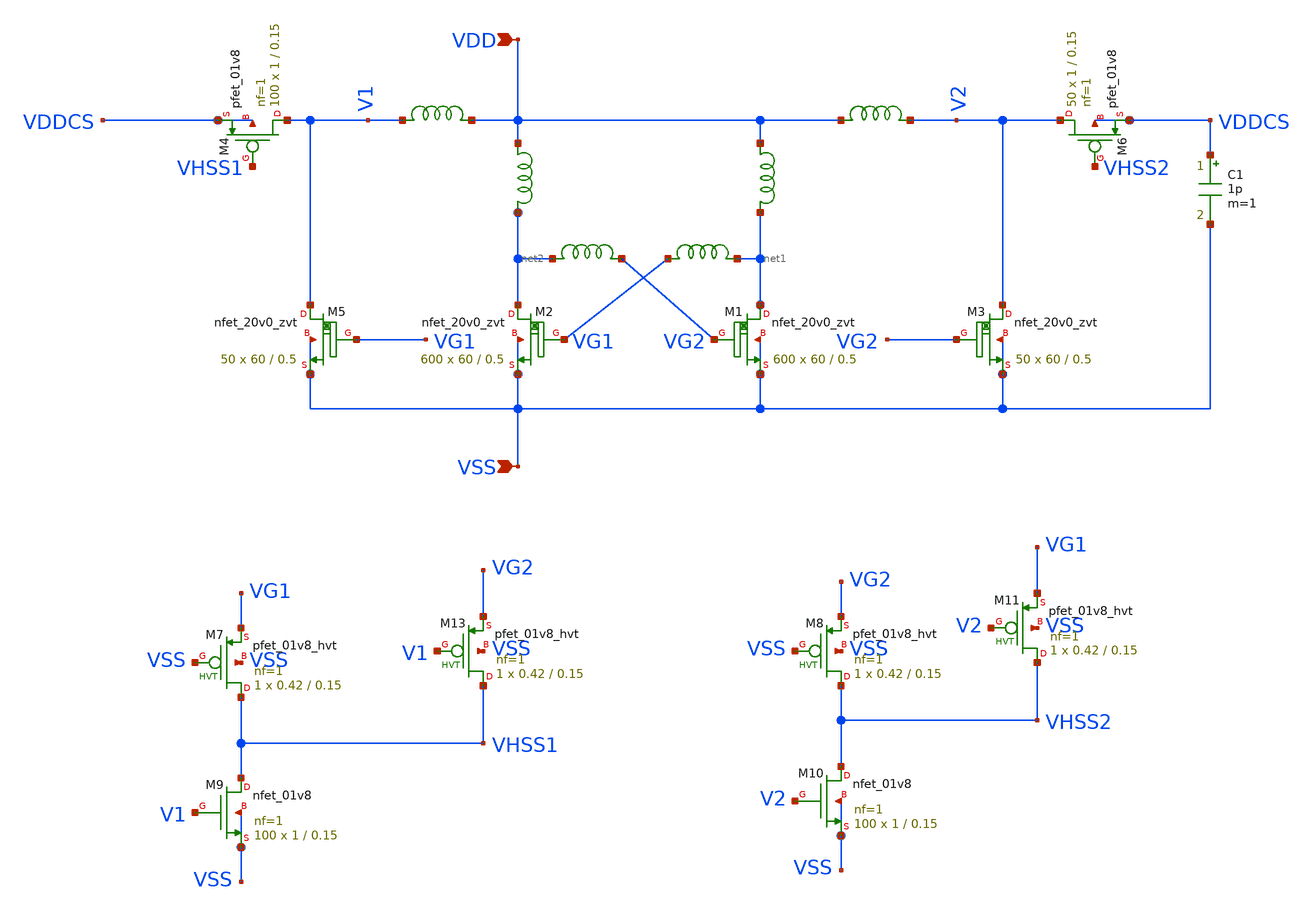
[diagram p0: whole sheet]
** sch_path: design/LELO_SVOD_SKY130A/LELO_EXSC.sch
**.subckt LELO_EXSC VSS VDD
*.ipin VSS
*.ipin VDD
x3 VDD net1 1812PS-102_imp
x4 VDD net2 1812PS-102_imp
XM1 net1 VG2 VSS VSS sky130_fd_pr__nfet_20v0_zvt W=60 L=0.5 m=600
XM2 net2 VG1 VSS VSS sky130_fd_pr__nfet_20v0_zvt W=60 L=0.5 m=600
x1 net2 VG2 1812PS-104_imp
x2 VG1 net1 1812PS-104_imp
XM3 V2 VG2 VSS VSS sky130_fd_pr__nfet_20v0_zvt W=60 L=0.5 m=50
C1 VDDCS VSS 1p m=1
XM5 V1 VG1 VSS VSS sky130_fd_pr__nfet_20v0_zvt W=60 L=0.5 m=50
XM4 V1 VHSS1 VDDCS VDDCS sky130_fd_pr__pfet_01v8 L=0.15 W=1 nf=1 ad='int((1 + 1)/2) * 1 / 1 * 0.29' as='int((1 + 2)/2) * 1 / 1 * 0.29'
+ pd='2*int((1 + 1)/2) * (1 / 1 + 0.29)' ps='2*int((1 + 2)/2) * (1 / 1 + 0.29)' nrd='0.29 / 1 ' nrs='0.29 / 1 '
+ sa=0 sb=0 sd=0 mult=100 m=100
XM6 V2 VHSS2 VDDCS VDDCS sky130_fd_pr__pfet_01v8 L=0.15 W=1 nf=1 ad='int((1 + 1)/2) * 1 / 1 * 0.29' as='int((1 + 2)/2) * 1 / 1 * 0.29'
+ pd='2*int((1 + 1)/2) * (1 / 1 + 0.29)' ps='2*int((1 + 2)/2) * (1 / 1 + 0.29)' nrd='0.29 / 1 ' nrs='0.29 / 1 '
+ sa=0 sb=0 sd=0 mult=50 m=50
XM13 VHSS1 V1 VG2 VSS sky130_fd_pr__pfet_01v8_hvt L=0.15 W=0.42 nf=1 ad='int((1 + 1)/2) * 0.42 / 1 * 0.29'
+ as='int((1 + 2)/2) * 0.42 / 1 * 0.29' pd='2*int((1 + 1)/2) * (0.42 / 1 + 0.29)' ps='2*int((1 + 2)/2) * (0.42 / 1 + 0.29)'
+ nrd='0.29 / 0.42 ' nrs='0.29 / 0.42 ' sa=0 sb=0 sd=0 mult=1 m=1
XM7 VHSS1 VSS VG1 VSS sky130_fd_pr__pfet_01v8_hvt L=0.15 W=0.42 nf=1 ad='int((1 + 1)/2) * 0.42 / 1 * 0.29'
+ as='int((1 + 2)/2) * 0.42 / 1 * 0.29' pd='2*int((1 + 1)/2) * (0.42 / 1 + 0.29)' ps='2*int((1 + 2)/2) * (0.42 / 1 + 0.29)'
+ nrd='0.29 / 0.42 ' nrs='0.29 / 0.42 ' sa=0 sb=0 sd=0 mult=1 m=1
XM8 VHSS2 VSS VG2 VSS sky130_fd_pr__pfet_01v8_hvt L=0.15 W=0.42 nf=1 ad='int((1 + 1)/2) * 0.42 / 1 * 0.29'
+ as='int((1 + 2)/2) * 0.42 / 1 * 0.29' pd='2*int((1 + 1)/2) * (0.42 / 1 + 0.29)' ps='2*int((1 + 2)/2) * (0.42 / 1 + 0.29)'
+ nrd='0.29 / 0.42 ' nrs='0.29 / 0.42 ' sa=0 sb=0 sd=0 mult=1 m=1
XM11 VHSS2 V2 VG1 VSS sky130_fd_pr__pfet_01v8_hvt L=0.15 W=0.42 nf=1 ad='int((1 + 1)/2) * 0.42 / 1 * 0.29'
+ as='int((1 + 2)/2) * 0.42 / 1 * 0.29' pd='2*int((1 + 1)/2) * (0.42 / 1 + 0.29)' ps='2*int((1 + 2)/2) * (0.42 / 1 + 0.29)'
+ nrd='0.29 / 0.42 ' nrs='0.29 / 0.42 ' sa=0 sb=0 sd=0 mult=1 m=1
XM9 VHSS1 V1 VSS VSS sky130_fd_pr__nfet_01v8 L=0.15 W=1 nf=1 ad='int((1 + 1)/2) * 1 / 1 * 0.29' as='int((1 + 2)/2) * 1 / 1 * 0.29'
+ pd='2*int((1 + 1)/2) * (1 / 1 + 0.29)' ps='2*int((1 + 2)/2) * (1 / 1 + 0.29)' nrd='0.29 / 1 ' nrs='0.29 / 1 '
+ sa=0 sb=0 sd=0 mult=100 m=100
XM10 VHSS2 V2 VSS VSS sky130_fd_pr__nfet_01v8 L=0.15 W=1 nf=1 ad='int((1 + 1)/2) * 1 / 1 * 0.29' as='int((1 + 2)/2) * 1 / 1 * 0.29'
+ pd='2*int((1 + 1)/2) * (1 / 1 + 0.29)' ps='2*int((1 + 2)/2) * (1 / 1 + 0.29)' nrd='0.29 / 1 ' nrs='0.29 / 1 '
+ sa=0 sb=0 sd=0 mult=100 m=100
x6 VDD V2 1812PS-334_imp
x5 V1 VDD 1812PS-334_imp
**.ends

* expanding   symbol:  LELO_SVOD_SKY130A/1812PS-102_imp.sym # of pins=2
** sym_path: design/LELO_SVOD_SKY130A/1812PS-102_imp.sym

.subckt 1812PS-102_imp port1 port2
X1 port1 port2 Model1D R1=60 R2=0.054 C= 0.15p K1=0.000001 K2=0.064 K3= 1u K4=1E-06 K5=0.000001 L=0
+ Is=0 a=0 L_Z0=0 L_EL=0 L_F0=0E6 PkZ=1282.46492
.ends 1812PS-102_imp

* expanding   symbol:  LELO_SVOD_SKY130A/1812PS-104_imp.sym # of pins=2
** sym_path: design/LELO_SVOD_SKY130A/1812PS-104_imp.sym

.subckt 1812PS-104_imp port1 port2
X1 port1 port2 Model1D R1=40 R2=1.3 C= 1.6p K1=0.000001 K2=13.98 K3= 100u K4=0.000001 K5=0.000001
+ L=0 Is=0 a=0 L_Z0=0 L_EL=0 L_F0=0E6 PkZ=48065.0165
.ends 1812PS-104_imp

* expanding   symbol:  LELO_SVOD_SKY130A/1812PS-334_imp.sym # of pins=2
** sym_path: design/LELO_SVOD_SKY130A/1812PS-334_imp.sym

.subckt 1812PS-334_imp port1 port2
X1 port1 port2 Model1D R1=75 R2=4.9 C= 2.43p K1=1E-06 K2=57.9 K3= 330u K4=0.000001 K5=0.000001 L=0
+ Is=0 a=0 L_Z0=0 L_EL=0 L_F0=0E6 PkZ=127597.141
.ends 1812PS-334_imp

.end
